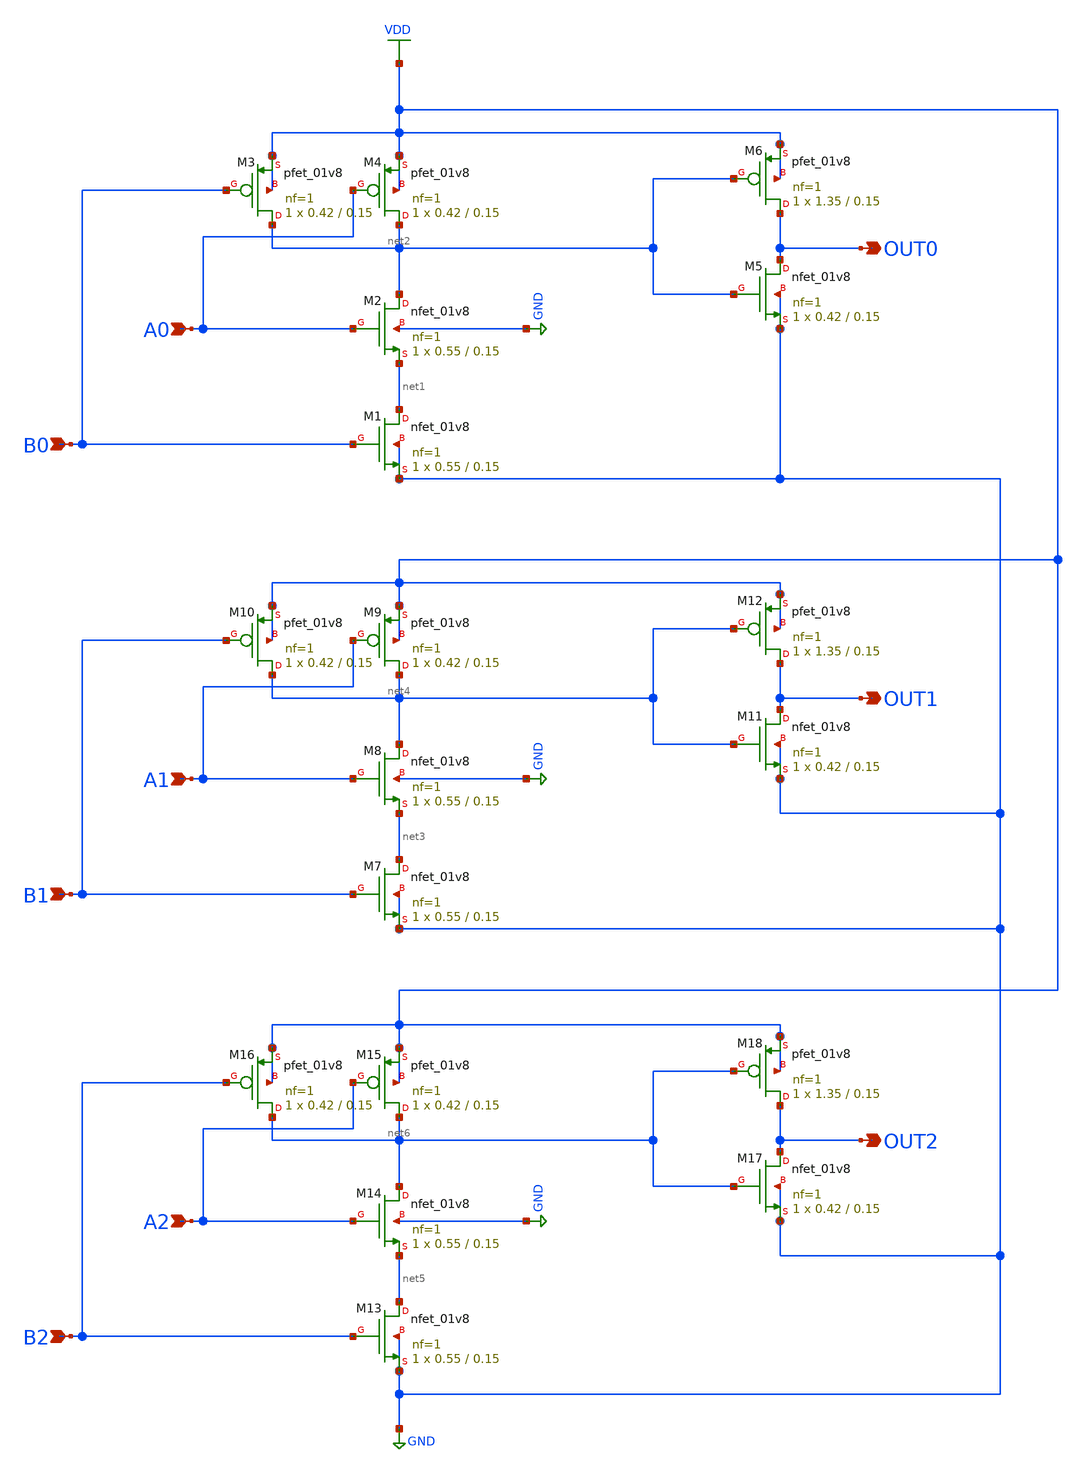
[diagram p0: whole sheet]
** sch_path: xschem/dec_cell_2.sch
**.subckt dec_cell_2 A0 B0 A1 B1 B2 A2 OUT0 OUT1 OUT2
*.ipin A0
*.ipin B0
*.ipin A1
*.ipin B1
*.ipin B2
*.ipin A2
*.opin OUT0
*.opin OUT1
*.opin OUT2
XM1 net1 B0 GND GND sky130_fd_pr__nfet_01v8 L=0.15 W=0.55 nf=1 ad='int((nf+1)/2) * W/nf * 0.29' as='int((nf+2)/2) * W/nf * 0.29'
+ pd='2*int((nf+1)/2) * (W/nf + 0.29)' ps='2*int((nf+2)/2) * (W/nf + 0.29)' nrd='0.29 / W' nrs='0.29 / W'
+ sa=0 sb=0 sd=0 mult=1 m=1
XM2 net2 A0 net1 GND sky130_fd_pr__nfet_01v8 L=0.15 W=0.55 nf=1 ad='int((nf+1)/2) * W/nf * 0.29' as='int((nf+2)/2) * W/nf * 0.29'
+ pd='2*int((nf+1)/2) * (W/nf + 0.29)' ps='2*int((nf+2)/2) * (W/nf + 0.29)' nrd='0.29 / W' nrs='0.29 / W'
+ sa=0 sb=0 sd=0 mult=1 m=1
XM4 net2 A0 VDD VDD sky130_fd_pr__pfet_01v8 L=0.15 W=0.42 nf=1 ad='int((nf+1)/2) * W/nf * 0.29' as='int((nf+2)/2) * W/nf * 0.29'
+ pd='2*int((nf+1)/2) * (W/nf + 0.29)' ps='2*int((nf+2)/2) * (W/nf + 0.29)' nrd='0.29 / W' nrs='0.29 / W'
+ sa=0 sb=0 sd=0 mult=1 m=1
XM3 net2 B0 VDD VDD sky130_fd_pr__pfet_01v8 L=0.15 W=0.42 nf=1 ad='int((nf+1)/2) * W/nf * 0.29' as='int((nf+2)/2) * W/nf * 0.29'
+ pd='2*int((nf+1)/2) * (W/nf + 0.29)' ps='2*int((nf+2)/2) * (W/nf + 0.29)' nrd='0.29 / W' nrs='0.29 / W'
+ sa=0 sb=0 sd=0 mult=1 m=1
XM5 OUT0 net2 GND GND sky130_fd_pr__nfet_01v8 L=0.15 W=0.42 nf=1 ad='int((nf+1)/2) * W/nf * 0.29' as='int((nf+2)/2) * W/nf * 0.29'
+ pd='2*int((nf+1)/2) * (W/nf + 0.29)' ps='2*int((nf+2)/2) * (W/nf + 0.29)' nrd='0.29 / W' nrs='0.29 / W'
+ sa=0 sb=0 sd=0 mult=1 m=1
XM6 OUT0 net2 VDD VDD sky130_fd_pr__pfet_01v8 L=0.15 W=1.35 nf=1 ad='int((nf+1)/2) * W/nf * 0.29' as='int((nf+2)/2) * W/nf * 0.29'
+ pd='2*int((nf+1)/2) * (W/nf + 0.29)' ps='2*int((nf+2)/2) * (W/nf + 0.29)' nrd='0.29 / W' nrs='0.29 / W'
+ sa=0 sb=0 sd=0 mult=1 m=1
XM7 net3 B1 GND GND sky130_fd_pr__nfet_01v8 L=0.15 W=0.55 nf=1 ad='int((nf+1)/2) * W/nf * 0.29' as='int((nf+2)/2) * W/nf * 0.29'
+ pd='2*int((nf+1)/2) * (W/nf + 0.29)' ps='2*int((nf+2)/2) * (W/nf + 0.29)' nrd='0.29 / W' nrs='0.29 / W'
+ sa=0 sb=0 sd=0 mult=1 m=1
XM8 net4 A1 net3 GND sky130_fd_pr__nfet_01v8 L=0.15 W=0.55 nf=1 ad='int((nf+1)/2) * W/nf * 0.29' as='int((nf+2)/2) * W/nf * 0.29'
+ pd='2*int((nf+1)/2) * (W/nf + 0.29)' ps='2*int((nf+2)/2) * (W/nf + 0.29)' nrd='0.29 / W' nrs='0.29 / W'
+ sa=0 sb=0 sd=0 mult=1 m=1
XM9 net4 A1 VDD VDD sky130_fd_pr__pfet_01v8 L=0.15 W=0.42 nf=1 ad='int((nf+1)/2) * W/nf * 0.29' as='int((nf+2)/2) * W/nf * 0.29'
+ pd='2*int((nf+1)/2) * (W/nf + 0.29)' ps='2*int((nf+2)/2) * (W/nf + 0.29)' nrd='0.29 / W' nrs='0.29 / W'
+ sa=0 sb=0 sd=0 mult=1 m=1
XM10 net4 B1 VDD VDD sky130_fd_pr__pfet_01v8 L=0.15 W=0.42 nf=1 ad='int((nf+1)/2) * W/nf * 0.29' as='int((nf+2)/2) * W/nf * 0.29'
+ pd='2*int((nf+1)/2) * (W/nf + 0.29)' ps='2*int((nf+2)/2) * (W/nf + 0.29)' nrd='0.29 / W' nrs='0.29 / W'
+ sa=0 sb=0 sd=0 mult=1 m=1
XM11 OUT1 net4 GND GND sky130_fd_pr__nfet_01v8 L=0.15 W=0.42 nf=1 ad='int((nf+1)/2) * W/nf * 0.29' as='int((nf+2)/2) * W/nf * 0.29'
+ pd='2*int((nf+1)/2) * (W/nf + 0.29)' ps='2*int((nf+2)/2) * (W/nf + 0.29)' nrd='0.29 / W' nrs='0.29 / W'
+ sa=0 sb=0 sd=0 mult=1 m=1
XM12 OUT1 net4 VDD VDD sky130_fd_pr__pfet_01v8 L=0.15 W=1.35 nf=1 ad='int((nf+1)/2) * W/nf * 0.29' as='int((nf+2)/2) * W/nf * 0.29'
+ pd='2*int((nf+1)/2) * (W/nf + 0.29)' ps='2*int((nf+2)/2) * (W/nf + 0.29)' nrd='0.29 / W' nrs='0.29 / W'
+ sa=0 sb=0 sd=0 mult=1 m=1
XM13 net5 B2 GND GND sky130_fd_pr__nfet_01v8 L=0.15 W=0.55 nf=1 ad='int((nf+1)/2) * W/nf * 0.29' as='int((nf+2)/2) * W/nf * 0.29'
+ pd='2*int((nf+1)/2) * (W/nf + 0.29)' ps='2*int((nf+2)/2) * (W/nf + 0.29)' nrd='0.29 / W' nrs='0.29 / W'
+ sa=0 sb=0 sd=0 mult=1 m=1
XM14 net6 A2 net5 GND sky130_fd_pr__nfet_01v8 L=0.15 W=0.55 nf=1 ad='int((nf+1)/2) * W/nf * 0.29' as='int((nf+2)/2) * W/nf * 0.29'
+ pd='2*int((nf+1)/2) * (W/nf + 0.29)' ps='2*int((nf+2)/2) * (W/nf + 0.29)' nrd='0.29 / W' nrs='0.29 / W'
+ sa=0 sb=0 sd=0 mult=1 m=1
XM15 net6 A2 VDD VDD sky130_fd_pr__pfet_01v8 L=0.15 W=0.42 nf=1 ad='int((nf+1)/2) * W/nf * 0.29' as='int((nf+2)/2) * W/nf * 0.29'
+ pd='2*int((nf+1)/2) * (W/nf + 0.29)' ps='2*int((nf+2)/2) * (W/nf + 0.29)' nrd='0.29 / W' nrs='0.29 / W'
+ sa=0 sb=0 sd=0 mult=1 m=1
XM16 net6 B2 VDD VDD sky130_fd_pr__pfet_01v8 L=0.15 W=0.42 nf=1 ad='int((nf+1)/2) * W/nf * 0.29' as='int((nf+2)/2) * W/nf * 0.29'
+ pd='2*int((nf+1)/2) * (W/nf + 0.29)' ps='2*int((nf+2)/2) * (W/nf + 0.29)' nrd='0.29 / W' nrs='0.29 / W'
+ sa=0 sb=0 sd=0 mult=1 m=1
XM17 OUT2 net6 GND GND sky130_fd_pr__nfet_01v8 L=0.15 W=0.42 nf=1 ad='int((nf+1)/2) * W/nf * 0.29' as='int((nf+2)/2) * W/nf * 0.29'
+ pd='2*int((nf+1)/2) * (W/nf + 0.29)' ps='2*int((nf+2)/2) * (W/nf + 0.29)' nrd='0.29 / W' nrs='0.29 / W'
+ sa=0 sb=0 sd=0 mult=1 m=1
XM18 OUT2 net6 VDD VDD sky130_fd_pr__pfet_01v8 L=0.15 W=1.35 nf=1 ad='int((nf+1)/2) * W/nf * 0.29' as='int((nf+2)/2) * W/nf * 0.29'
+ pd='2*int((nf+1)/2) * (W/nf + 0.29)' ps='2*int((nf+2)/2) * (W/nf + 0.29)' nrd='0.29 / W' nrs='0.29 / W'
+ sa=0 sb=0 sd=0 mult=1 m=1
**.ends
.GLOBAL GND
.GLOBAL VDD
.end
